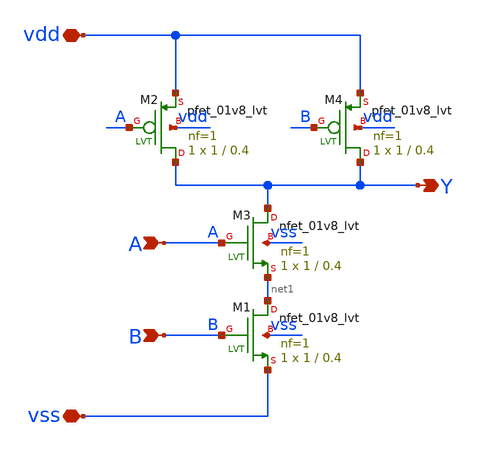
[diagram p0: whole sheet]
** sch_path: xschem/logic/nand.sch
**.subckt nand vdd vss A Y B
*.iopin vdd
*.iopin vss
*.ipin A
*.opin Y
*.ipin B
XM1 net1 B vss vss sky130_fd_pr__nfet_01v8_lvt L=0.4 W=1 nf=1 ad='int((nf+1)/2) * W/nf * 0.29' as='int((nf+2)/2) * W/nf * 0.29'
+ pd='2*int((nf+1)/2) * (W/nf + 0.29)' ps='2*int((nf+2)/2) * (W/nf + 0.29)' nrd='0.29 / W' nrs='0.29 / W'
+ sa=0 sb=0 sd=0 mult=1 m=1
XM2 Y A vdd vdd sky130_fd_pr__pfet_01v8_lvt L=0.4 W=1 nf=1 ad='int((nf+1)/2) * W/nf * 0.29' as='int((nf+2)/2) * W/nf * 0.29'
+ pd='2*int((nf+1)/2) * (W/nf + 0.29)' ps='2*int((nf+2)/2) * (W/nf + 0.29)' nrd='0.29 / W' nrs='0.29 / W'
+ sa=0 sb=0 sd=0 mult=1 m=1
XM3 Y A net1 vss sky130_fd_pr__nfet_01v8_lvt L=0.4 W=1 nf=1 ad='int((nf+1)/2) * W/nf * 0.29' as='int((nf+2)/2) * W/nf * 0.29'
+ pd='2*int((nf+1)/2) * (W/nf + 0.29)' ps='2*int((nf+2)/2) * (W/nf + 0.29)' nrd='0.29 / W' nrs='0.29 / W'
+ sa=0 sb=0 sd=0 mult=1 m=1
XM4 Y B vdd vdd sky130_fd_pr__pfet_01v8_lvt L=0.4 W=1 nf=1 ad='int((nf+1)/2) * W/nf * 0.29' as='int((nf+2)/2) * W/nf * 0.29'
+ pd='2*int((nf+1)/2) * (W/nf + 0.29)' ps='2*int((nf+2)/2) * (W/nf + 0.29)' nrd='0.29 / W' nrs='0.29 / W'
+ sa=0 sb=0 sd=0 mult=1 m=1
**.ends
.end
